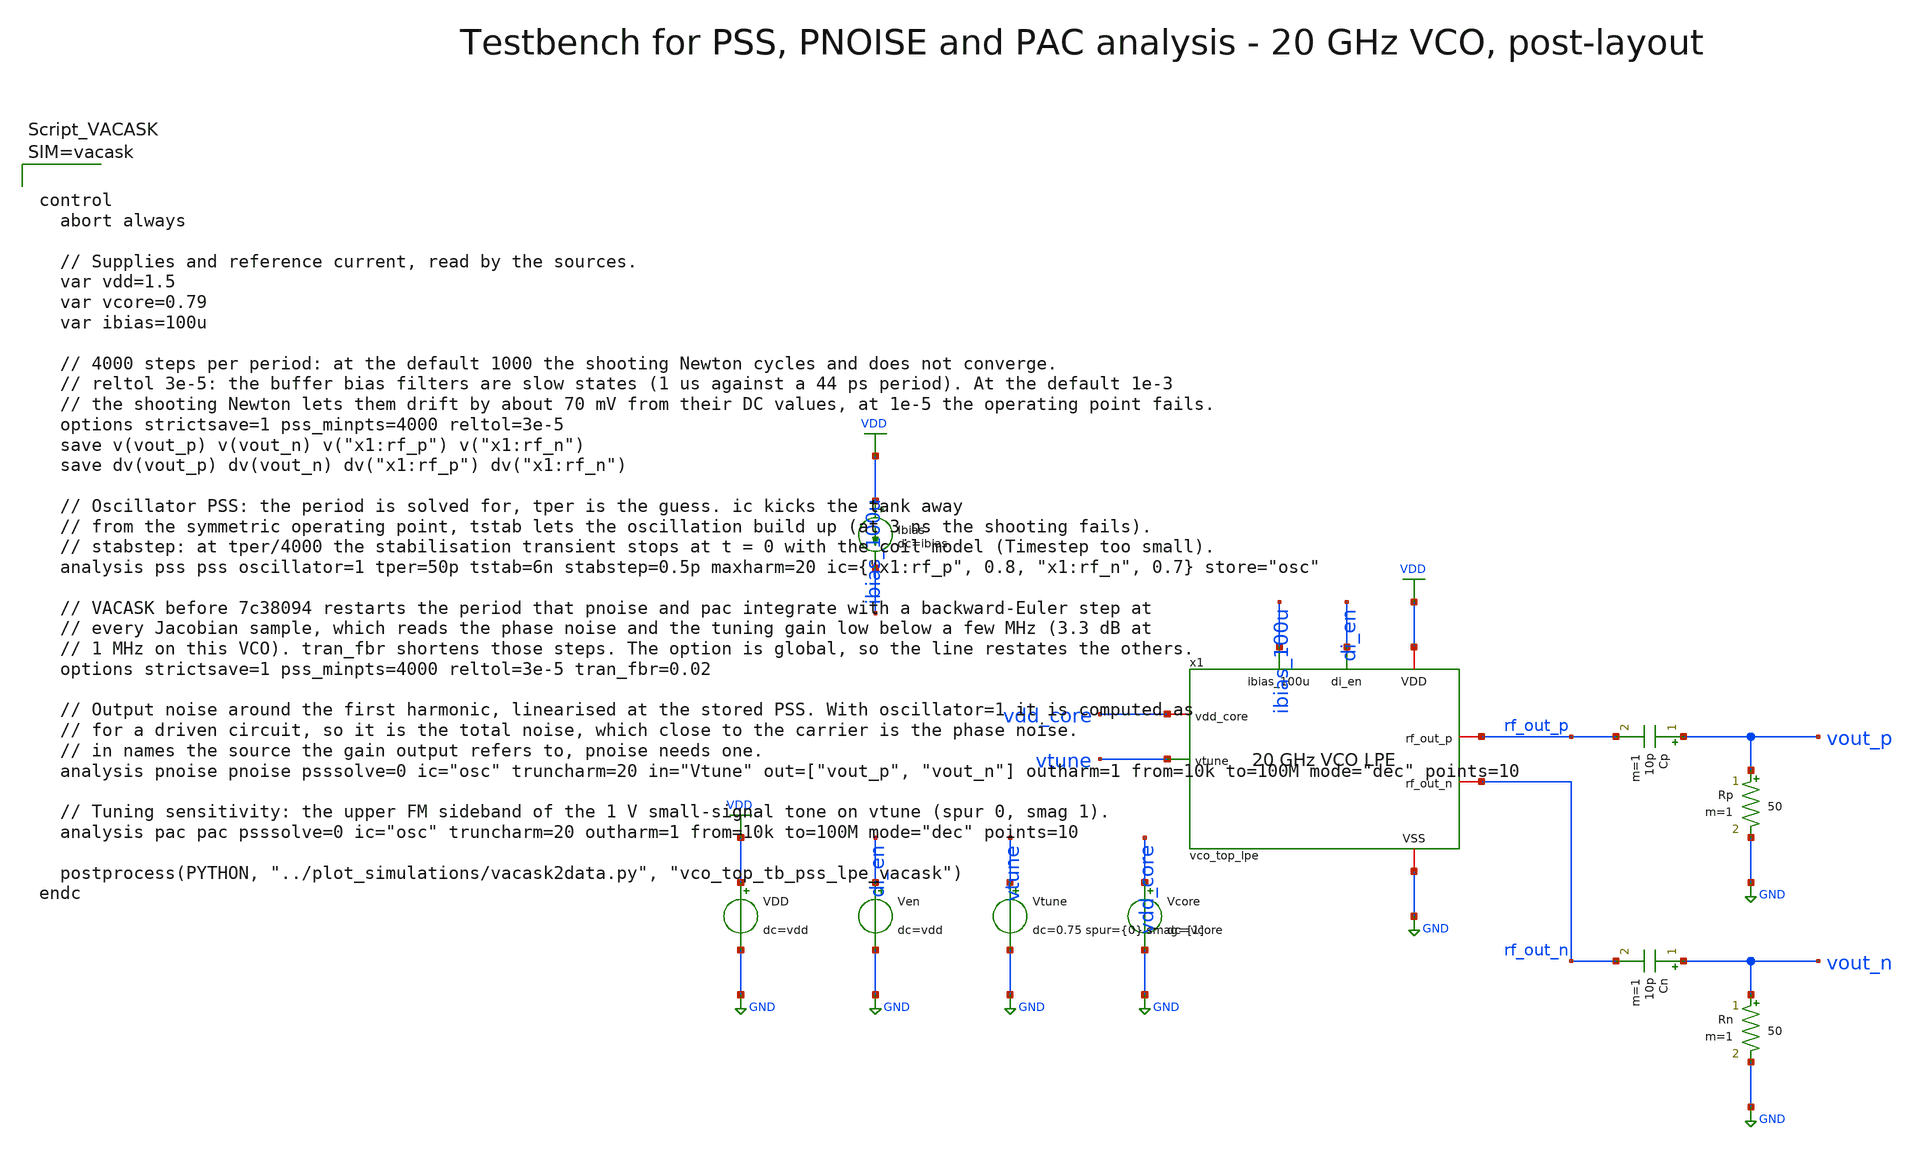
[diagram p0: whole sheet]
** sch_path: macros/vco/testbenches/xschem/vco_top_tb_pss_lpe_vacask.sch
**.subckt vco_top_tb_pss_lpe_vacask
x1 ibias_100u di_en VDD GND vdd_core vtune rf_out_p rf_out_n vco_top_lpe
Vcore vdd_core GND dc=vcore
Cp vout_p rf_out_p 10p m=1
Rp vout_p GND 50 m=1
Cn vout_n rf_out_n 10p m=1
Rn vout_n GND 50 m=1
VDD VDD GND dc=vdd
Ven di_en GND dc=vdd
Vtune vtune GND dc=0.75 spur={0} smag=[1]
Ibias VDD ibias_100u dc=ibias
**** begin user architecture code






**** end user architecture code
**.ends
.GLOBAL VDD
.GLOBAL GND
.end
